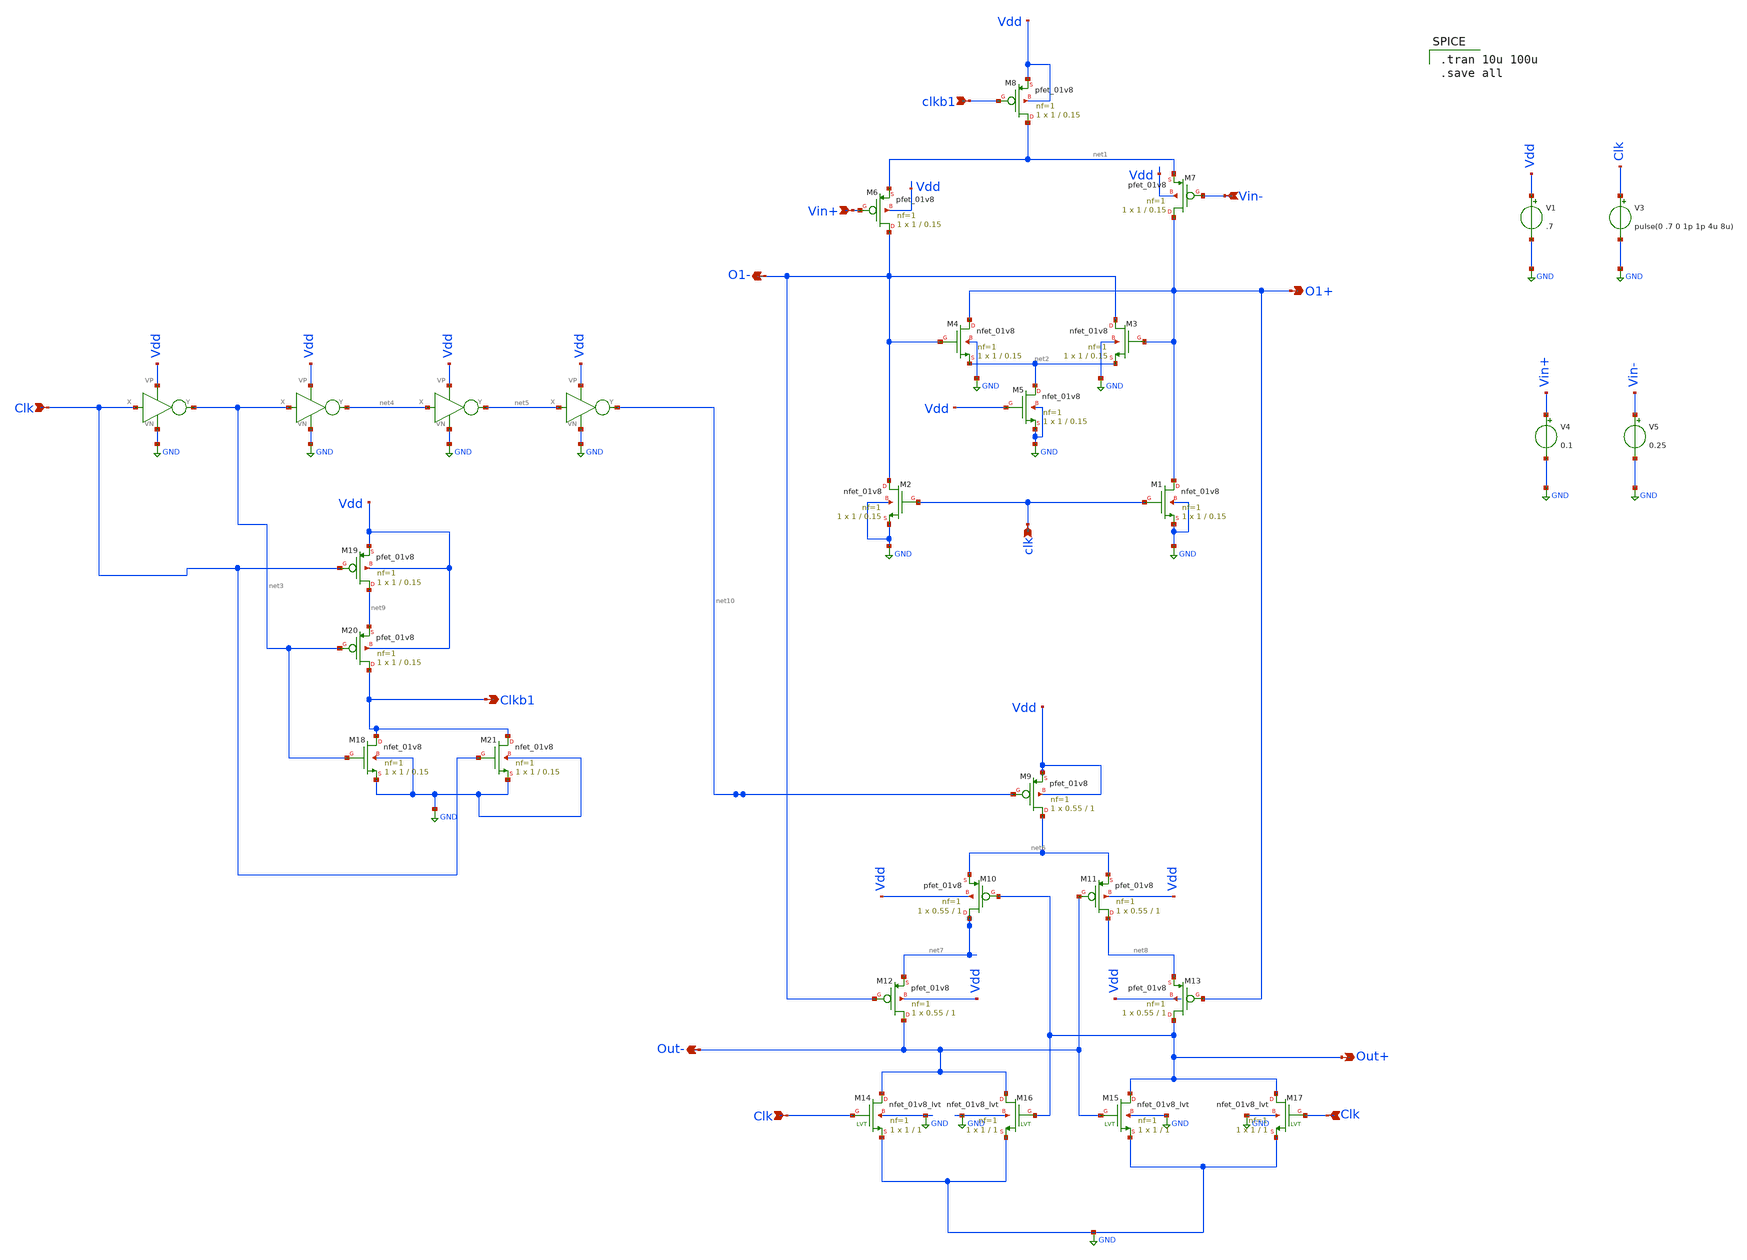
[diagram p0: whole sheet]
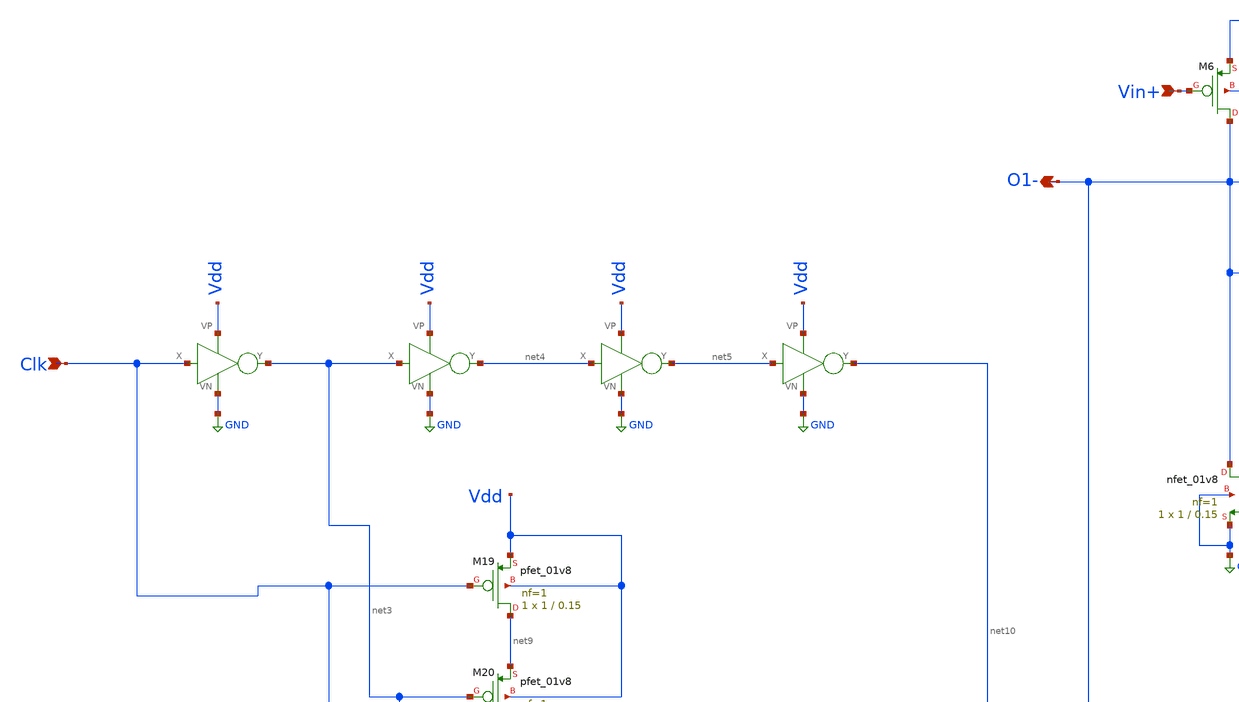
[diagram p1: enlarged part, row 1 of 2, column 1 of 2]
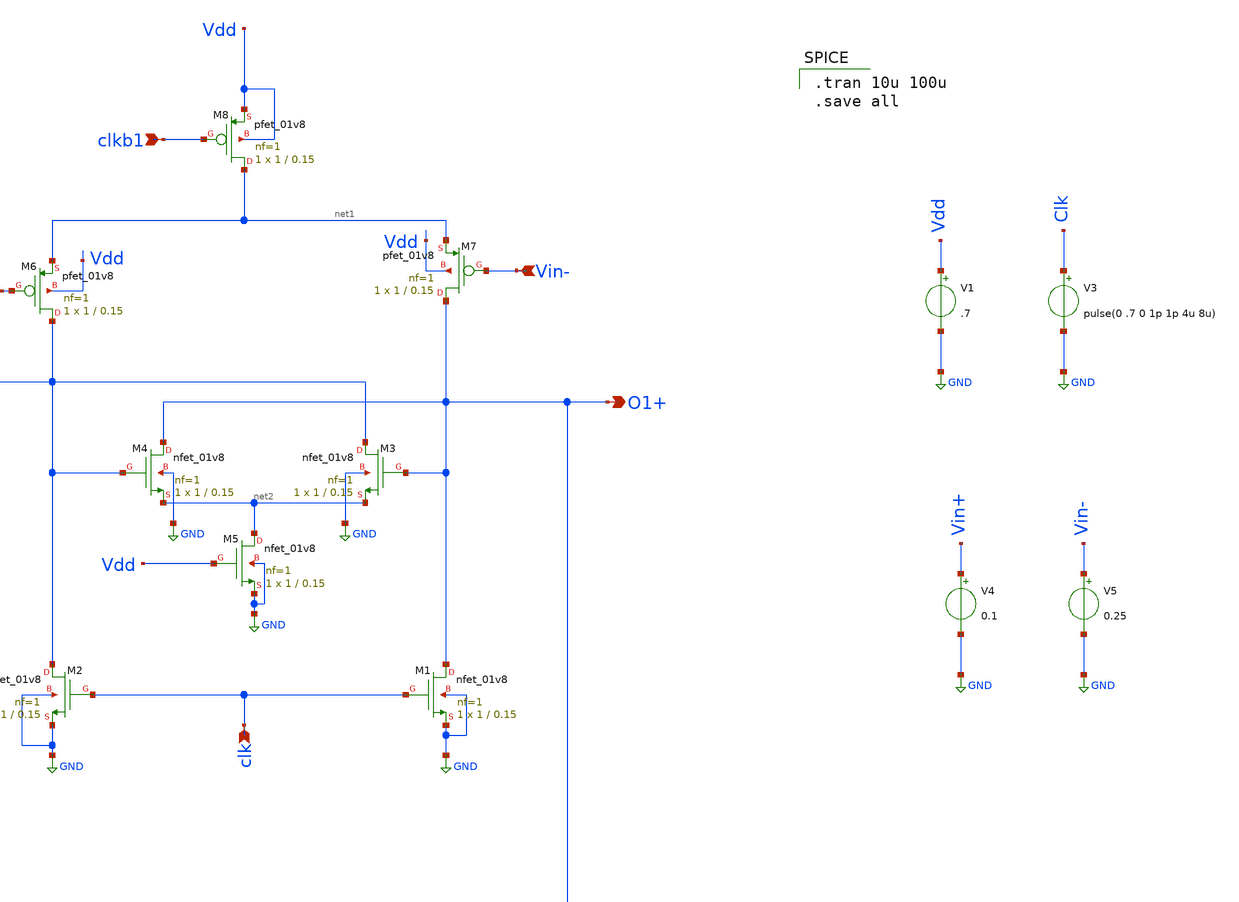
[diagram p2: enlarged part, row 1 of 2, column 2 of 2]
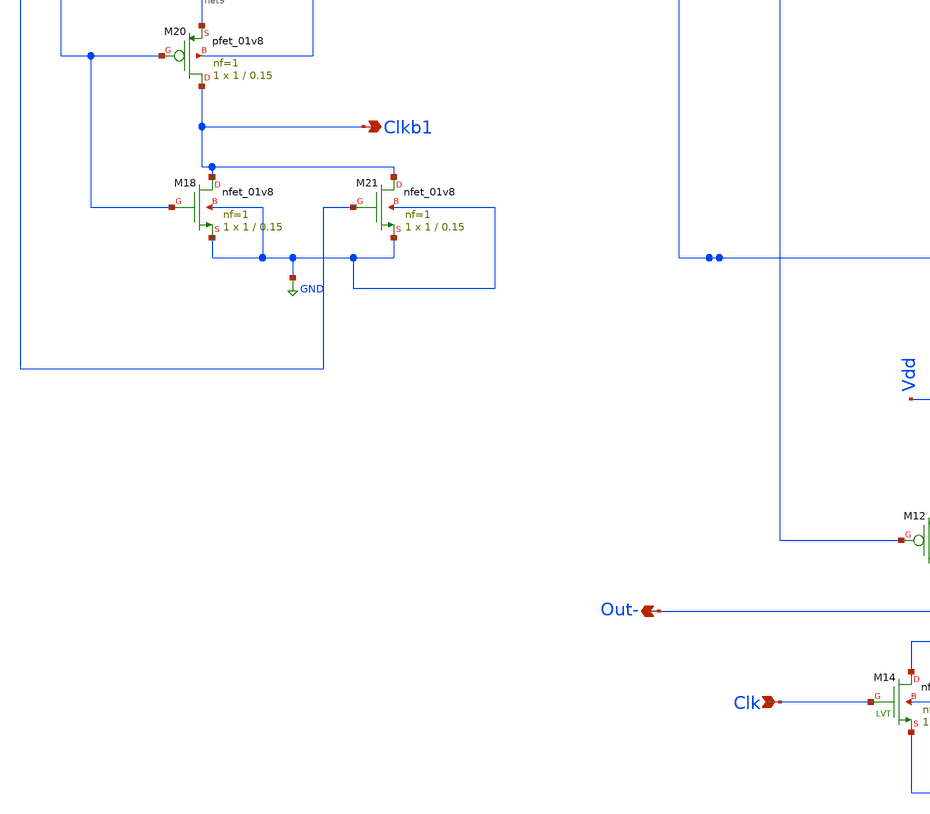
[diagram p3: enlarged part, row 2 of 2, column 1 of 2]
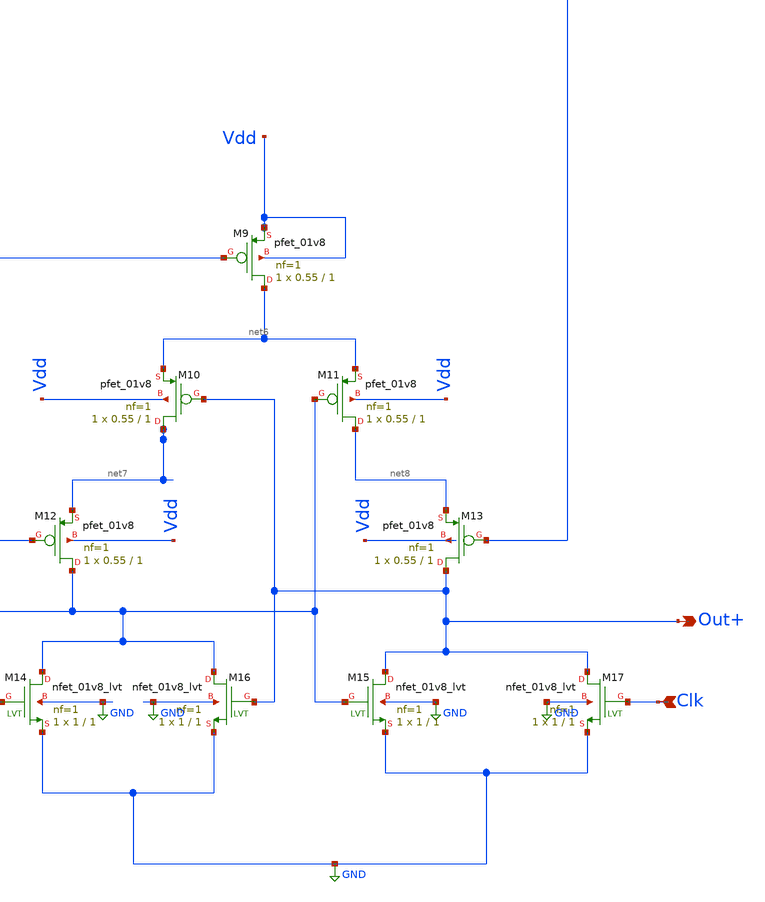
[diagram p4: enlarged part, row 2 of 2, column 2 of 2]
** sch_path: Blocks/main_comparator/p1.sch
**.subckt p1 clkb1 Vin+ Vin- O1+ O1- clk Clk Out+ Out- Clk Clk Clkb1
*.ipin clkb1
*.ipin Vin+
*.ipin Vin-
*.opin O1+
*.opin O1-
*.ipin clk
*.ipin Clk
*.opin Out+
*.opin Out-
*.ipin Clk
*.ipin Clk
*.opin Clkb1
XM1 O1+ clk GND GND sky130_fd_pr__nfet_01v8 L=0.15 W=1 nf=1 ad='int((nf+1)/2) * W/nf * 0.29' as='int((nf+2)/2) * W/nf * 0.29'
+ pd='2*int((nf+1)/2) * (W/nf + 0.29)' ps='2*int((nf+2)/2) * (W/nf + 0.29)' nrd='0.29 / W' nrs='0.29 / W'
+ sa=0 sb=0 sd=0 mult=1 m=1
XM2 O1- clk GND GND sky130_fd_pr__nfet_01v8 L=0.15 W=1 nf=1 ad='int((nf+1)/2) * W/nf * 0.29' as='int((nf+2)/2) * W/nf * 0.29'
+ pd='2*int((nf+1)/2) * (W/nf + 0.29)' ps='2*int((nf+2)/2) * (W/nf + 0.29)' nrd='0.29 / W' nrs='0.29 / W'
+ sa=0 sb=0 sd=0 mult=1 m=1
XM3 O1- O1+ net2 GND sky130_fd_pr__nfet_01v8 L=0.15 W=1 nf=1 ad='int((nf+1)/2) * W/nf * 0.29' as='int((nf+2)/2) * W/nf * 0.29'
+ pd='2*int((nf+1)/2) * (W/nf + 0.29)' ps='2*int((nf+2)/2) * (W/nf + 0.29)' nrd='0.29 / W' nrs='0.29 / W'
+ sa=0 sb=0 sd=0 mult=1 m=1
XM4 O1+ O1- net2 GND sky130_fd_pr__nfet_01v8 L=0.15 W=1 nf=1 ad='int((nf+1)/2) * W/nf * 0.29' as='int((nf+2)/2) * W/nf * 0.29'
+ pd='2*int((nf+1)/2) * (W/nf + 0.29)' ps='2*int((nf+2)/2) * (W/nf + 0.29)' nrd='0.29 / W' nrs='0.29 / W'
+ sa=0 sb=0 sd=0 mult=1 m=1
XM5 net2 Vdd GND GND sky130_fd_pr__nfet_01v8 L=0.15 W=1 nf=1 ad='int((nf+1)/2) * W/nf * 0.29' as='int((nf+2)/2) * W/nf * 0.29'
+ pd='2*int((nf+1)/2) * (W/nf + 0.29)' ps='2*int((nf+2)/2) * (W/nf + 0.29)' nrd='0.29 / W' nrs='0.29 / W'
+ sa=0 sb=0 sd=0 mult=1 m=1
XM6 O1- Vin+ net1 Vdd sky130_fd_pr__pfet_01v8 L=0.15 W=1 nf=1 ad='int((nf+1)/2) * W/nf * 0.29' as='int((nf+2)/2) * W/nf * 0.29'
+ pd='2*int((nf+1)/2) * (W/nf + 0.29)' ps='2*int((nf+2)/2) * (W/nf + 0.29)' nrd='0.29 / W' nrs='0.29 / W'
+ sa=0 sb=0 sd=0 mult=1 m=1
XM7 O1+ Vin- net1 Vdd sky130_fd_pr__pfet_01v8 L=0.15 W=1 nf=1 ad='int((nf+1)/2) * W/nf * 0.29' as='int((nf+2)/2) * W/nf * 0.29'
+ pd='2*int((nf+1)/2) * (W/nf + 0.29)' ps='2*int((nf+2)/2) * (W/nf + 0.29)' nrd='0.29 / W' nrs='0.29 / W'
+ sa=0 sb=0 sd=0 mult=1 m=1
XM8 net1 clkb1 Vdd Vdd sky130_fd_pr__pfet_01v8 L=0.15 W=1 nf=1 ad='int((nf+1)/2) * W/nf * 0.29' as='int((nf+2)/2) * W/nf * 0.29'
+ pd='2*int((nf+1)/2) * (W/nf + 0.29)' ps='2*int((nf+2)/2) * (W/nf + 0.29)' nrd='0.29 / W' nrs='0.29 / W'
+ sa=0 sb=0 sd=0 mult=1 m=1
V1 Vdd GND .7
V3 Clk GND pulse(0 .7 0 1p 1p 4u 8u)
V4 Vin+ GND 0.1
V5 Vin- GND 0.25
XM9 net6 net10 Vdd Vdd sky130_fd_pr__pfet_01v8 L=1 W=0.55 nf=1 ad='W * 0.29' as='W * 0.29' pd='W + 2 * 0.29'
+ ps='W + 2 * 0.29' nrd=0 nrs=0 sa=0 sb=0 sd=0 mult=1 m=1
XM10 net7 Out+ net6 Vdd sky130_fd_pr__pfet_01v8 L=1 W=0.55 nf=1 ad='W * 0.29' as='W * 0.29' pd='W + 2 * 0.29'
+ ps='W + 2 * 0.29' nrd=0 nrs=0 sa=0 sb=0 sd=0 mult=1 m=1
XM11 net8 Out- net6 Vdd sky130_fd_pr__pfet_01v8 L=1 W=0.55 nf=1 ad='W * 0.29' as='W * 0.29' pd='W + 2 * 0.29'
+ ps='W + 2 * 0.29' nrd=0 nrs=0 sa=0 sb=0 sd=0 mult=1 m=1
XM12 Out- O1- net7 Vdd sky130_fd_pr__pfet_01v8 L=1 W=0.55 nf=1 ad='W * 0.29' as='W * 0.29' pd='W + 2 * 0.29'
+ ps='W + 2 * 0.29' nrd=0 nrs=0 sa=0 sb=0 sd=0 mult=1 m=1
XM13 Out+ O1+ net8 Vdd sky130_fd_pr__pfet_01v8 L=1 W=0.55 nf=1 ad='W * 0.29' as='W * 0.29' pd='W + 2 * 0.29'
+ ps='W + 2 * 0.29' nrd=0 nrs=0 sa=0 sb=0 sd=0 mult=1 m=1
XM14 Out- Clk GND GND sky130_fd_pr__nfet_01v8_lvt L=1 W=1 nf=1 ad='W * 0.29' as='W * 0.29' pd='2*(W + 0.29)'
+ ps='2*(W + 0.29)' nrd=0 nrs=0 sa=0 sb=0 sd=0 mult=1 m=1
XM15 Out+ Out- GND GND sky130_fd_pr__nfet_01v8_lvt L=1 W=1 nf=1 ad='W * 0.29' as='W * 0.29' pd='2*(W + 0.29)'
+ ps='2*(W + 0.29)' nrd=0 nrs=0 sa=0 sb=0 sd=0 mult=1 m=1
XM16 Out- Out+ GND GND sky130_fd_pr__nfet_01v8_lvt L=1 W=1 nf=1 ad='W * 0.29' as='W * 0.29' pd='2*(W + 0.29)'
+ ps='2*(W + 0.29)' nrd=0 nrs=0 sa=0 sb=0 sd=0 mult=1 m=1
XM17 Out+ Clk GND GND sky130_fd_pr__nfet_01v8_lvt L=1 W=1 nf=1 ad='W * 0.29' as='W * 0.29' pd='2*(W + 0.29)'
+ ps='2*(W + 0.29)' nrd=0 nrs=0 sa=0 sb=0 sd=0 mult=1 m=1
XM18 Clkb1 net3 GND GND sky130_fd_pr__nfet_01v8 L=0.15 W=1 nf=1 ad='int((nf+1)/2) * W/nf * 0.29' as='int((nf+2)/2) * W/nf * 0.29'
+ pd='2*int((nf+1)/2) * (W/nf + 0.29)' ps='2*int((nf+2)/2) * (W/nf + 0.29)' nrd='0.29 / W' nrs='0.29 / W'
+ sa=0 sb=0 sd=0 mult=1 m=1
XM19 net9 Clk Vdd Vdd sky130_fd_pr__pfet_01v8 L=0.15 W=1 nf=1 ad='int((nf+1)/2) * W/nf * 0.29' as='int((nf+2)/2) * W/nf * 0.29'
+ pd='2*int((nf+1)/2) * (W/nf + 0.29)' ps='2*int((nf+2)/2) * (W/nf + 0.29)' nrd='0.29 / W' nrs='0.29 / W'
+ sa=0 sb=0 sd=0 mult=1 m=1
XM20 Clkb1 net3 net9 Vdd sky130_fd_pr__pfet_01v8 L=0.15 W=1 nf=1 ad='int((nf+1)/2) * W/nf * 0.29' as='int((nf+2)/2) * W/nf * 0.29'
+ pd='2*int((nf+1)/2) * (W/nf + 0.29)' ps='2*int((nf+2)/2) * (W/nf + 0.29)' nrd='0.29 / W' nrs='0.29 / W'
+ sa=0 sb=0 sd=0 mult=1 m=1
XM21 Clkb1 Clk GND GND sky130_fd_pr__nfet_01v8 L=0.15 W=1 nf=1 ad='int((nf+1)/2) * W/nf * 0.29' as='int((nf+2)/2) * W/nf * 0.29'
+ pd='2*int((nf+1)/2) * (W/nf + 0.29)' ps='2*int((nf+2)/2) * (W/nf + 0.29)' nrd='0.29 / W' nrs='0.29 / W'
+ sa=0 sb=0 sd=0 mult=1 m=1
x1 Clk net3 Vdd GND INV
x2 net3 net4 Vdd GND INV
x3 net4 net5 Vdd GND INV
x4 net5 net10 Vdd GND INV
**** begin user architecture code

** opencircuitdesign pdks install
.lib $::SKYWATER_MODELS/sky130.lib.spice tt



.tran 10u 100u
.save all

**** end user architecture code
**.ends
.GLOBAL GND
.end
